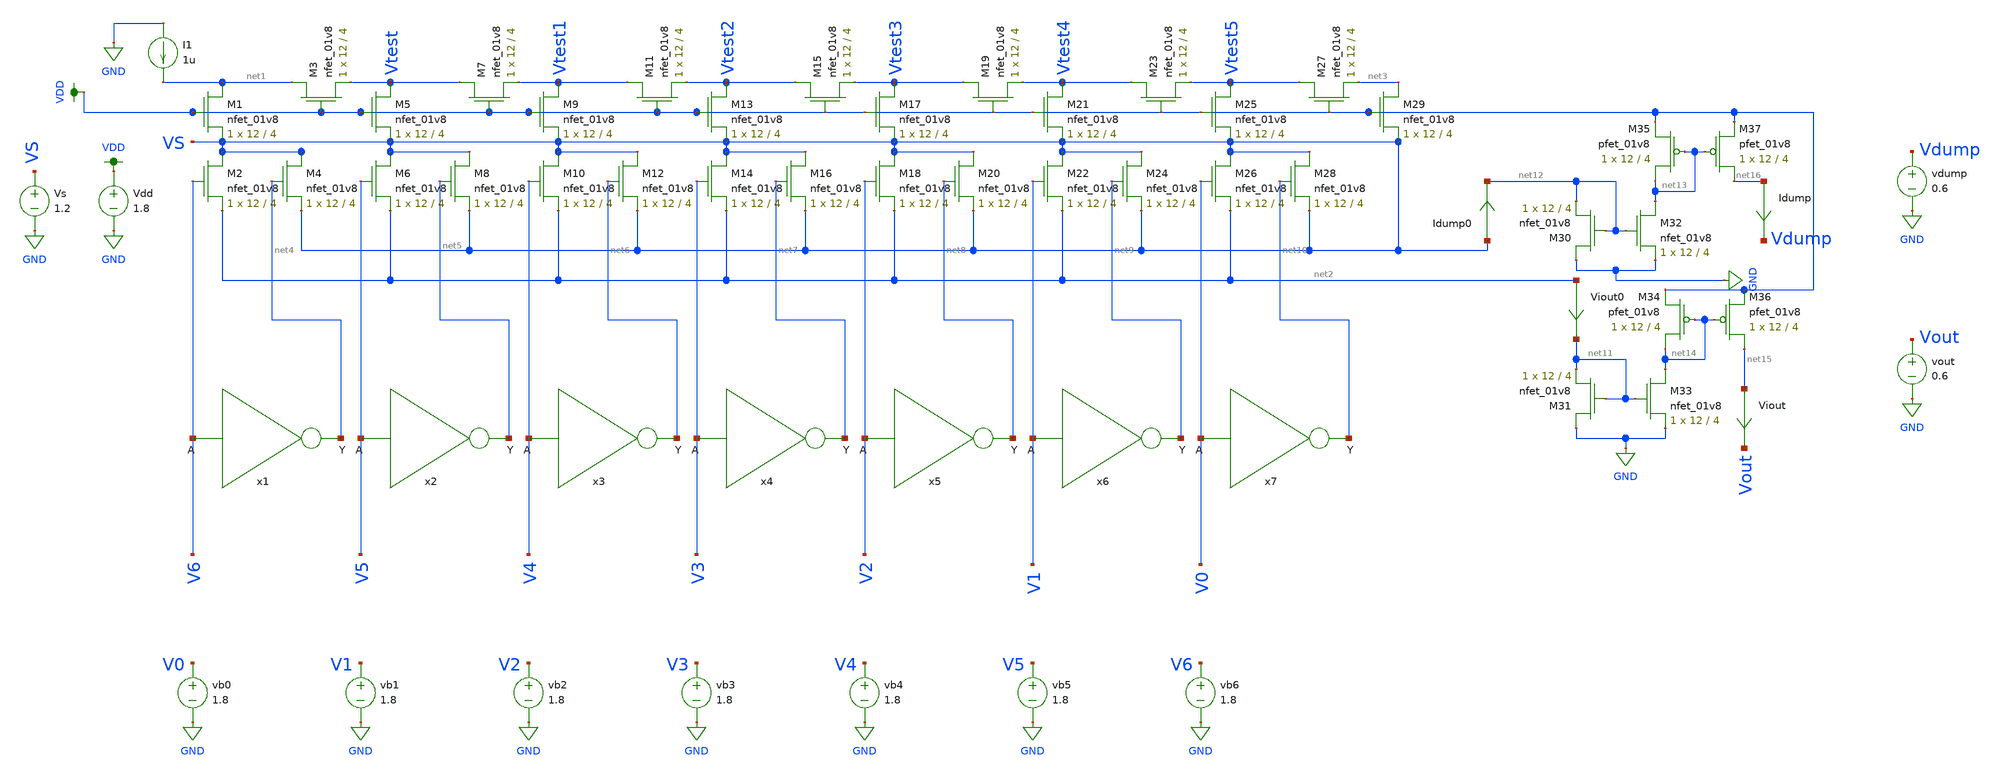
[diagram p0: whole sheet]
** sch_path: xschem/old_files/ladder_dac_simulation.sch
**.subckt ladder_dac_simulation
XM1 net1 VDD VS GND sky130_fd_pr__nfet_01v8 L=4 W=12 nf=1 ad='int((nf+1)/2) * W/nf * 0.29' as='int((nf+2)/2) * W/nf * 0.29'
+ pd='2*int((nf+1)/2) * (W/nf + 0.29)' ps='2*int((nf+2)/2) * (W/nf + 0.29)' nrd='0.29 / W' nrs='0.29 / W'
+ sa=0 sb=0 sd=0 mult=1 m=1
XM3 net1 VDD Vtest GND sky130_fd_pr__nfet_01v8 L=4 W=12 nf=1 ad='int((nf+1)/2) * W/nf * 0.29' as='int((nf+2)/2) * W/nf * 0.29'
+ pd='2*int((nf+1)/2) * (W/nf + 0.29)' ps='2*int((nf+2)/2) * (W/nf + 0.29)' nrd='0.29 / W' nrs='0.29 / W'
+ sa=0 sb=0 sd=0 mult=1 m=1
XM5 Vtest VDD VS GND sky130_fd_pr__nfet_01v8 L=4 W=12 nf=1 ad='int((nf+1)/2) * W/nf * 0.29' as='int((nf+2)/2) * W/nf * 0.29'
+ pd='2*int((nf+1)/2) * (W/nf + 0.29)' ps='2*int((nf+2)/2) * (W/nf + 0.29)' nrd='0.29 / W' nrs='0.29 / W'
+ sa=0 sb=0 sd=0 mult=1 m=1
XM7 Vtest VDD Vtest1 GND sky130_fd_pr__nfet_01v8 L=4 W=12 nf=1 ad='int((nf+1)/2) * W/nf * 0.29' as='int((nf+2)/2) * W/nf * 0.29'
+ pd='2*int((nf+1)/2) * (W/nf + 0.29)' ps='2*int((nf+2)/2) * (W/nf + 0.29)' nrd='0.29 / W' nrs='0.29 / W'
+ sa=0 sb=0 sd=0 mult=1 m=1
XM6 VS V5 net2 GND sky130_fd_pr__nfet_01v8 L=4 W=12 nf=1 ad='int((nf+1)/2) * W/nf * 0.29' as='int((nf+2)/2) * W/nf * 0.29'
+ pd='2*int((nf+1)/2) * (W/nf + 0.29)' ps='2*int((nf+2)/2) * (W/nf + 0.29)' nrd='0.29 / W' nrs='0.29 / W'
+ sa=0 sb=0 sd=0 mult=1 m=1
XM8 VS net5 VS GND sky130_fd_pr__nfet_01v8 L=4 W=12 nf=1 ad='int((nf+1)/2) * W/nf * 0.29' as='int((nf+2)/2) * W/nf * 0.29'
+ pd='2*int((nf+1)/2) * (W/nf + 0.29)' ps='2*int((nf+2)/2) * (W/nf + 0.29)' nrd='0.29 / W' nrs='0.29 / W'
+ sa=0 sb=0 sd=0 mult=1 m=1
XM2 VS V6 net2 GND sky130_fd_pr__nfet_01v8 L=4 W=12 nf=1 ad='int((nf+1)/2) * W/nf * 0.29' as='int((nf+2)/2) * W/nf * 0.29'
+ pd='2*int((nf+1)/2) * (W/nf + 0.29)' ps='2*int((nf+2)/2) * (W/nf + 0.29)' nrd='0.29 / W' nrs='0.29 / W'
+ sa=0 sb=0 sd=0 mult=1 m=1
XM4 VS net4 VS GND sky130_fd_pr__nfet_01v8 L=4 W=12 nf=1 ad='int((nf+1)/2) * W/nf * 0.29' as='int((nf+2)/2) * W/nf * 0.29'
+ pd='2*int((nf+1)/2) * (W/nf + 0.29)' ps='2*int((nf+2)/2) * (W/nf + 0.29)' nrd='0.29 / W' nrs='0.29 / W'
+ sa=0 sb=0 sd=0 mult=1 m=1
XM9 Vtest1 VDD VS GND sky130_fd_pr__nfet_01v8 L=4 W=12 nf=1 ad='int((nf+1)/2) * W/nf * 0.29' as='int((nf+2)/2) * W/nf * 0.29'
+ pd='2*int((nf+1)/2) * (W/nf + 0.29)' ps='2*int((nf+2)/2) * (W/nf + 0.29)' nrd='0.29 / W' nrs='0.29 / W'
+ sa=0 sb=0 sd=0 mult=1 m=1
XM11 Vtest1 VDD Vtest2 GND sky130_fd_pr__nfet_01v8 L=4 W=12 nf=1 ad='int((nf+1)/2) * W/nf * 0.29' as='int((nf+2)/2) * W/nf * 0.29'
+ pd='2*int((nf+1)/2) * (W/nf + 0.29)' ps='2*int((nf+2)/2) * (W/nf + 0.29)' nrd='0.29 / W' nrs='0.29 / W'
+ sa=0 sb=0 sd=0 mult=1 m=1
XM10 VS V4 net2 GND sky130_fd_pr__nfet_01v8 L=4 W=12 nf=1 ad='int((nf+1)/2) * W/nf * 0.29' as='int((nf+2)/2) * W/nf * 0.29'
+ pd='2*int((nf+1)/2) * (W/nf + 0.29)' ps='2*int((nf+2)/2) * (W/nf + 0.29)' nrd='0.29 / W' nrs='0.29 / W'
+ sa=0 sb=0 sd=0 mult=1 m=1
XM12 VS net6 VS GND sky130_fd_pr__nfet_01v8 L=4 W=12 nf=1 ad='int((nf+1)/2) * W/nf * 0.29' as='int((nf+2)/2) * W/nf * 0.29'
+ pd='2*int((nf+1)/2) * (W/nf + 0.29)' ps='2*int((nf+2)/2) * (W/nf + 0.29)' nrd='0.29 / W' nrs='0.29 / W'
+ sa=0 sb=0 sd=0 mult=1 m=1
XM13 Vtest2 VDD VS GND sky130_fd_pr__nfet_01v8 L=4 W=12 nf=1 ad='int((nf+1)/2) * W/nf * 0.29' as='int((nf+2)/2) * W/nf * 0.29'
+ pd='2*int((nf+1)/2) * (W/nf + 0.29)' ps='2*int((nf+2)/2) * (W/nf + 0.29)' nrd='0.29 / W' nrs='0.29 / W'
+ sa=0 sb=0 sd=0 mult=1 m=1
XM15 Vtest2 VDD Vtest3 GND sky130_fd_pr__nfet_01v8 L=4 W=12 nf=1 ad='int((nf+1)/2) * W/nf * 0.29' as='int((nf+2)/2) * W/nf * 0.29'
+ pd='2*int((nf+1)/2) * (W/nf + 0.29)' ps='2*int((nf+2)/2) * (W/nf + 0.29)' nrd='0.29 / W' nrs='0.29 / W'
+ sa=0 sb=0 sd=0 mult=1 m=1
XM14 VS V3 net2 GND sky130_fd_pr__nfet_01v8 L=4 W=12 nf=1 ad='int((nf+1)/2) * W/nf * 0.29' as='int((nf+2)/2) * W/nf * 0.29'
+ pd='2*int((nf+1)/2) * (W/nf + 0.29)' ps='2*int((nf+2)/2) * (W/nf + 0.29)' nrd='0.29 / W' nrs='0.29 / W'
+ sa=0 sb=0 sd=0 mult=1 m=1
XM16 VS net7 VS GND sky130_fd_pr__nfet_01v8 L=4 W=12 nf=1 ad='int((nf+1)/2) * W/nf * 0.29' as='int((nf+2)/2) * W/nf * 0.29'
+ pd='2*int((nf+1)/2) * (W/nf + 0.29)' ps='2*int((nf+2)/2) * (W/nf + 0.29)' nrd='0.29 / W' nrs='0.29 / W'
+ sa=0 sb=0 sd=0 mult=1 m=1
XM17 Vtest3 VDD VS GND sky130_fd_pr__nfet_01v8 L=4 W=12 nf=1 ad='int((nf+1)/2) * W/nf * 0.29' as='int((nf+2)/2) * W/nf * 0.29'
+ pd='2*int((nf+1)/2) * (W/nf + 0.29)' ps='2*int((nf+2)/2) * (W/nf + 0.29)' nrd='0.29 / W' nrs='0.29 / W'
+ sa=0 sb=0 sd=0 mult=1 m=1
XM19 Vtest3 VDD Vtest4 GND sky130_fd_pr__nfet_01v8 L=4 W=12 nf=1 ad='int((nf+1)/2) * W/nf * 0.29' as='int((nf+2)/2) * W/nf * 0.29'
+ pd='2*int((nf+1)/2) * (W/nf + 0.29)' ps='2*int((nf+2)/2) * (W/nf + 0.29)' nrd='0.29 / W' nrs='0.29 / W'
+ sa=0 sb=0 sd=0 mult=1 m=1
XM18 VS V2 net2 GND sky130_fd_pr__nfet_01v8 L=4 W=12 nf=1 ad='int((nf+1)/2) * W/nf * 0.29' as='int((nf+2)/2) * W/nf * 0.29'
+ pd='2*int((nf+1)/2) * (W/nf + 0.29)' ps='2*int((nf+2)/2) * (W/nf + 0.29)' nrd='0.29 / W' nrs='0.29 / W'
+ sa=0 sb=0 sd=0 mult=1 m=1
XM20 VS net8 VS GND sky130_fd_pr__nfet_01v8 L=4 W=12 nf=1 ad='int((nf+1)/2) * W/nf * 0.29' as='int((nf+2)/2) * W/nf * 0.29'
+ pd='2*int((nf+1)/2) * (W/nf + 0.29)' ps='2*int((nf+2)/2) * (W/nf + 0.29)' nrd='0.29 / W' nrs='0.29 / W'
+ sa=0 sb=0 sd=0 mult=1 m=1
XM21 Vtest4 VDD VS GND sky130_fd_pr__nfet_01v8 L=4 W=12 nf=1 ad='int((nf+1)/2) * W/nf * 0.29' as='int((nf+2)/2) * W/nf * 0.29'
+ pd='2*int((nf+1)/2) * (W/nf + 0.29)' ps='2*int((nf+2)/2) * (W/nf + 0.29)' nrd='0.29 / W' nrs='0.29 / W'
+ sa=0 sb=0 sd=0 mult=1 m=1
XM23 Vtest4 VDD Vtest5 GND sky130_fd_pr__nfet_01v8 L=4 W=12 nf=1 ad='int((nf+1)/2) * W/nf * 0.29' as='int((nf+2)/2) * W/nf * 0.29'
+ pd='2*int((nf+1)/2) * (W/nf + 0.29)' ps='2*int((nf+2)/2) * (W/nf + 0.29)' nrd='0.29 / W' nrs='0.29 / W'
+ sa=0 sb=0 sd=0 mult=1 m=1
XM22 VS V1 net2 GND sky130_fd_pr__nfet_01v8 L=4 W=12 nf=1 ad='int((nf+1)/2) * W/nf * 0.29' as='int((nf+2)/2) * W/nf * 0.29'
+ pd='2*int((nf+1)/2) * (W/nf + 0.29)' ps='2*int((nf+2)/2) * (W/nf + 0.29)' nrd='0.29 / W' nrs='0.29 / W'
+ sa=0 sb=0 sd=0 mult=1 m=1
XM24 VS net9 VS GND sky130_fd_pr__nfet_01v8 L=4 W=12 nf=1 ad='int((nf+1)/2) * W/nf * 0.29' as='int((nf+2)/2) * W/nf * 0.29'
+ pd='2*int((nf+1)/2) * (W/nf + 0.29)' ps='2*int((nf+2)/2) * (W/nf + 0.29)' nrd='0.29 / W' nrs='0.29 / W'
+ sa=0 sb=0 sd=0 mult=1 m=1
XM25 Vtest5 VDD VS GND sky130_fd_pr__nfet_01v8 L=4 W=12 nf=1 ad='int((nf+1)/2) * W/nf * 0.29' as='int((nf+2)/2) * W/nf * 0.29'
+ pd='2*int((nf+1)/2) * (W/nf + 0.29)' ps='2*int((nf+2)/2) * (W/nf + 0.29)' nrd='0.29 / W' nrs='0.29 / W'
+ sa=0 sb=0 sd=0 mult=1 m=1
XM27 Vtest5 VDD net3 GND sky130_fd_pr__nfet_01v8 L=4 W=12 nf=1 ad='int((nf+1)/2) * W/nf * 0.29' as='int((nf+2)/2) * W/nf * 0.29'
+ pd='2*int((nf+1)/2) * (W/nf + 0.29)' ps='2*int((nf+2)/2) * (W/nf + 0.29)' nrd='0.29 / W' nrs='0.29 / W'
+ sa=0 sb=0 sd=0 mult=1 m=1
XM26 VS V0 net2 GND sky130_fd_pr__nfet_01v8 L=4 W=12 nf=1 ad='int((nf+1)/2) * W/nf * 0.29' as='int((nf+2)/2) * W/nf * 0.29'
+ pd='2*int((nf+1)/2) * (W/nf + 0.29)' ps='2*int((nf+2)/2) * (W/nf + 0.29)' nrd='0.29 / W' nrs='0.29 / W'
+ sa=0 sb=0 sd=0 mult=1 m=1
XM28 VS net10 VS GND sky130_fd_pr__nfet_01v8 L=4 W=12 nf=1 ad='int((nf+1)/2) * W/nf * 0.29' as='int((nf+2)/2) * W/nf * 0.29'
+ pd='2*int((nf+1)/2) * (W/nf + 0.29)' ps='2*int((nf+2)/2) * (W/nf + 0.29)' nrd='0.29 / W' nrs='0.29 / W'
+ sa=0 sb=0 sd=0 mult=1 m=1
XM29 net3 VDD VS GND sky130_fd_pr__nfet_01v8 L=4 W=12 nf=1 ad='int((nf+1)/2) * W/nf * 0.29' as='int((nf+2)/2) * W/nf * 0.29'
+ pd='2*int((nf+1)/2) * (W/nf + 0.29)' ps='2*int((nf+2)/2) * (W/nf + 0.29)' nrd='0.29 / W' nrs='0.29 / W'
+ sa=0 sb=0 sd=0 mult=1 m=1
x1 net4 V6 inverter
x2 net5 V5 inverter
x3 net6 V4 inverter
x4 net7 V3 inverter
x5 net8 V2 inverter
x6 net9 V1 inverter
x7 net10 V0 inverter
XM30 GND net12 net12 GND sky130_fd_pr__nfet_01v8 L=4 W=12 nf=1 ad='int((nf+1)/2) * W/nf * 0.29' as='int((nf+2)/2) * W/nf * 0.29'
+ pd='2*int((nf+1)/2) * (W/nf + 0.29)' ps='2*int((nf+2)/2) * (W/nf + 0.29)' nrd='0.29 / W' nrs='0.29 / W'
+ sa=0 sb=0 sd=0 mult=1 m=1
XM31 GND net11 net11 GND sky130_fd_pr__nfet_01v8 L=4 W=12 nf=1 ad='int((nf+1)/2) * W/nf * 0.29' as='int((nf+2)/2) * W/nf * 0.29'
+ pd='2*int((nf+1)/2) * (W/nf + 0.29)' ps='2*int((nf+2)/2) * (W/nf + 0.29)' nrd='0.29 / W' nrs='0.29 / W'
+ sa=0 sb=0 sd=0 mult=1 m=1
XM32 net13 net12 GND GND sky130_fd_pr__nfet_01v8 L=4 W=12 nf=1 ad='int((nf+1)/2) * W/nf * 0.29' as='int((nf+2)/2) * W/nf * 0.29'
+ pd='2*int((nf+1)/2) * (W/nf + 0.29)' ps='2*int((nf+2)/2) * (W/nf + 0.29)' nrd='0.29 / W' nrs='0.29 / W'
+ sa=0 sb=0 sd=0 mult=1 m=1
XM33 net14 net11 GND GND sky130_fd_pr__nfet_01v8 L=4 W=12 nf=1 ad='int((nf+1)/2) * W/nf * 0.29' as='int((nf+2)/2) * W/nf * 0.29'
+ pd='2*int((nf+1)/2) * (W/nf + 0.29)' ps='2*int((nf+2)/2) * (W/nf + 0.29)' nrd='0.29 / W' nrs='0.29 / W'
+ sa=0 sb=0 sd=0 mult=1 m=1
XM35 net13 net13 VDD VDD sky130_fd_pr__pfet_01v8 L=4 W=12 nf=1 ad='int((nf+1)/2) * W/nf * 0.29' as='int((nf+2)/2) * W/nf * 0.29'
+ pd='2*int((nf+1)/2) * (W/nf + 0.29)' ps='2*int((nf+2)/2) * (W/nf + 0.29)' nrd='0.29 / W' nrs='0.29 / W'
+ sa=0 sb=0 sd=0 mult=1 m=1
XM37 net16 net13 VDD VDD sky130_fd_pr__pfet_01v8 L=4 W=12 nf=1 ad='int((nf+1)/2) * W/nf * 0.29' as='int((nf+2)/2) * W/nf * 0.29'
+ pd='2*int((nf+1)/2) * (W/nf + 0.29)' ps='2*int((nf+2)/2) * (W/nf + 0.29)' nrd='0.29 / W' nrs='0.29 / W'
+ sa=0 sb=0 sd=0 mult=1 m=1
XM34 net14 net14 VDD VDD sky130_fd_pr__pfet_01v8 L=4 W=12 nf=1 ad='int((nf+1)/2) * W/nf * 0.29' as='int((nf+2)/2) * W/nf * 0.29'
+ pd='2*int((nf+1)/2) * (W/nf + 0.29)' ps='2*int((nf+2)/2) * (W/nf + 0.29)' nrd='0.29 / W' nrs='0.29 / W'
+ sa=0 sb=0 sd=0 mult=1 m=1
XM36 net15 net14 VDD VDD sky130_fd_pr__pfet_01v8 L=4 W=12 nf=1 ad='int((nf+1)/2) * W/nf * 0.29' as='int((nf+2)/2) * W/nf * 0.29'
+ pd='2*int((nf+1)/2) * (W/nf + 0.29)' ps='2*int((nf+2)/2) * (W/nf + 0.29)' nrd='0.29 / W' nrs='0.29 / W'
+ sa=0 sb=0 sd=0 mult=1 m=1
I1 GND net1 1u
Vdd VDD GND 1.8
vb0 V0 GND 1.8
vb1 V1 GND 1.8
vb2 V2 GND 1.8
vb3 V3 GND 1.8
vb4 V4 GND 1.8
vb5 V5 GND 1.8
vb6 V6 GND 1.8
vdump Vdump GND 0.6
vout Vout GND 0.6
Idump net16 Vdump 0
.save i(idump)
Viout net15 Vout 0
.save i(viout)
Idump0 VS net12 0
.save i(idump0)
Viout0 net2 net11 0
.save i(viout0)
Vs VS GND 1.2
**** begin user architecture code

.option wnflag=1
.param MC_SWITCH=0.0
.lib ~/skywater/skywater-pdk/libraries/sky130_fd_pr_ngspice/latest/models/sky130.lib.spice tt



.control
  set wr_vecnames
  set wr_singlescale
  let code = 0
  while code < 128
    if code eq 0
      let b0 = 0
    else
      let b0 = code % 2
    end
    if floor(code / 2) eq 0
      let b1 = 0
    else
      let b1 = floor(code / 2) % 2
    end
    if floor(code / 4) eq 0
      let b2 = 0
    else
      let b2 = floor(code / 4) % 2
    end
    if floor(code / 8) eq 0
      let b3 = 0
    else
      let b3 = floor(code / 8) % 2
    end
    if floor(code / 16) eq 0
      let b4 = 0
    else
      let b4 = floor(code / 16) % 2
    end
    if floor(code / 32) eq 0
      let b5 = 0
    else
      let b5 = floor(code / 32) % 2
    end
    if floor(code / 64) eq 0
      let b6 = 0
    else
      let b6 = floor(code / 64) % 2
    end
    alter Vb0 1.8*$&b0
    alter Vb1 1.8*$&b1
    alter Vb2 1.8*$&b2
    alter Vb3 1.8*$&b3
    alter Vb4 1.8*$&b4
    alter Vb5 1.8*$&b5
    alter Vb6 1.8*$&b6
    save all
    op
    wrdata ~/Documents/DAC-VLSI/simulation_results/ladder_dac_simulation_andrew.txt v(b0) v(b1)
+ v(b2) v(b3) v(b4) v(b5) v(b6) i(Viout) v(Vtest) v(Vtest1) v(Vtest2) v(Vtest3) v(Vtest4) v(Vtest5)
    if code eq 0
      set appendwrite
      set wr_vecnames = FALSE
    end
    let code = code + 1
  end
  quit
.endc

**** end user architecture code
**.ends

* expanding   symbol:  ./inverter.sym # of pins=2
** sym_path: xschem/old_files/inverter.sym
** sch_path: xschem/old_files/inverter.sch
.subckt inverter Y A
*.ipin A
*.opin Y
XM1 Y A VDD VDD sky130_fd_pr__pfet_01v8 L=0.15 W=1 nf=1 ad='int((nf+1)/2) * W/nf * 0.29' as='int((nf+2)/2) * W/nf * 0.29'
+ pd='2*int((nf+1)/2) * (W/nf + 0.29)' ps='2*int((nf+2)/2) * (W/nf + 0.29)' nrd='0.29 / W' nrs='0.29 / W'
+ sa=0 sb=0 sd=0 mult=1 m=1
XM2 Y A GND GND sky130_fd_pr__nfet_01v8 L=0.15 W=1 nf=1 ad='int((nf+1)/2) * W/nf * 0.29' as='int((nf+2)/2) * W/nf * 0.29'
+ pd='2*int((nf+1)/2) * (W/nf + 0.29)' ps='2*int((nf+2)/2) * (W/nf + 0.29)' nrd='0.29 / W' nrs='0.29 / W'
+ sa=0 sb=0 sd=0 mult=1 m=1
.ends

.GLOBAL VDD
.GLOBAL GND
.end
